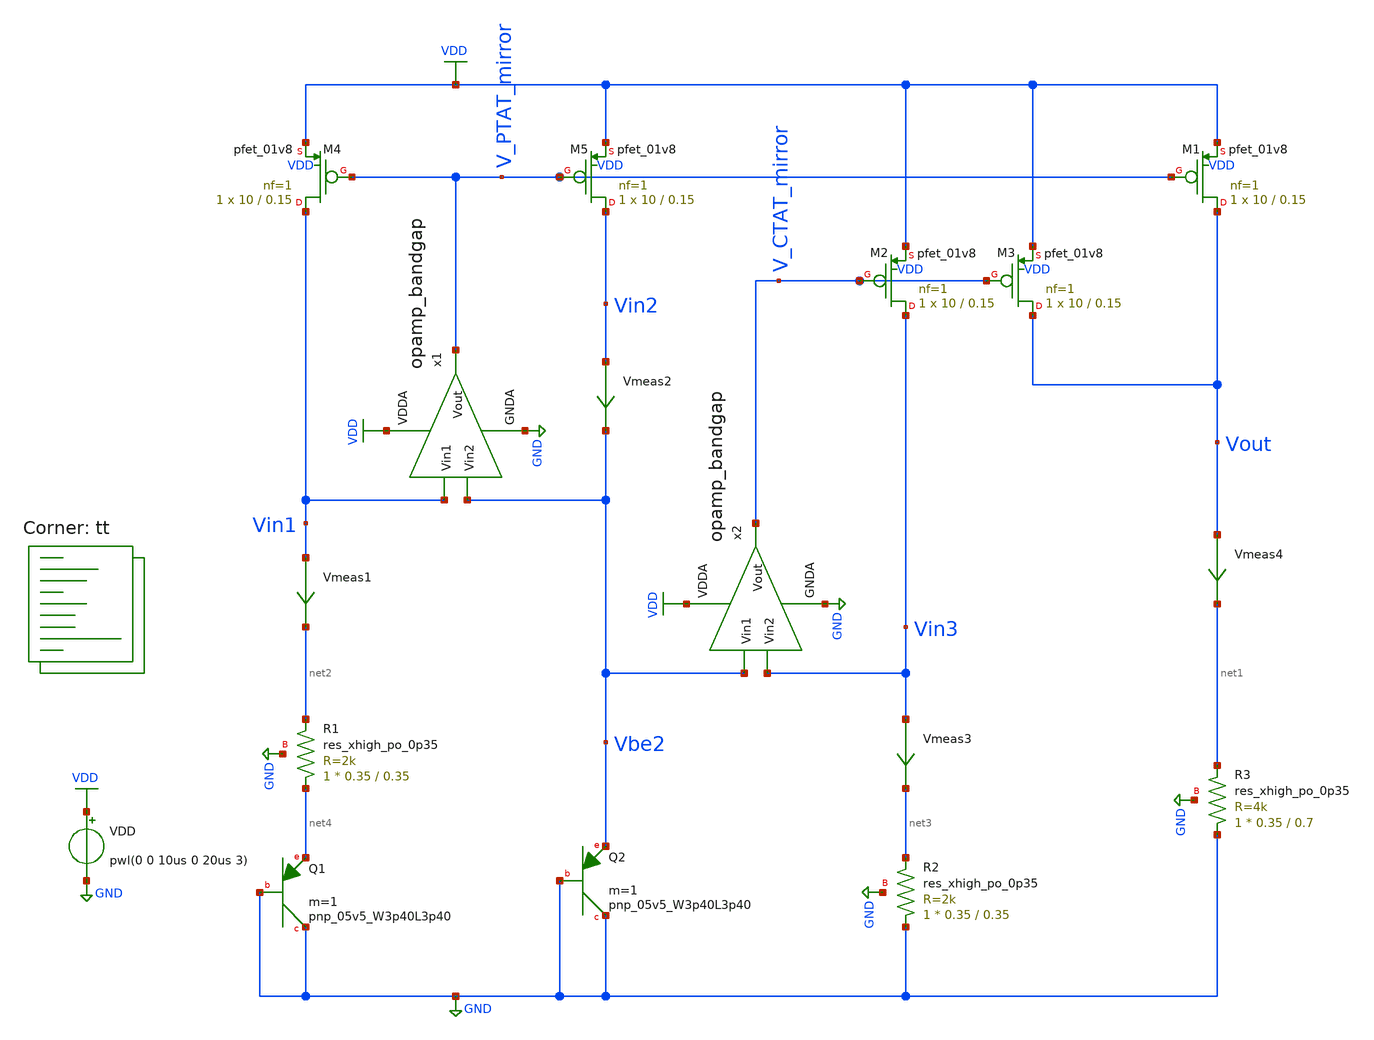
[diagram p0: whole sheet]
** sch_path: projects/pll/bandgapref/xschem_ngspice/mos_bandgap4.sch
**.subckt mos_bandgap4
XM4 Vin1 V_PTAT_mirror VDD VDD sky130_fd_pr__pfet_01v8 L=0.15 W=10 nf=1 ad='int((nf+1)/2) * W/nf * 0.29'
+ as='int((nf+2)/2) * W/nf * 0.29' pd='2*int((nf+1)/2) * (W/nf + 0.29)' ps='2*int((nf+2)/2) * (W/nf + 0.29)'
+ nrd='0.29 / W' nrs='0.29 / W' sa=0 sb=0 sd=0 mult=1 m=1
XM5 Vin2 V_PTAT_mirror VDD VDD sky130_fd_pr__pfet_01v8 L=0.15 W=10 nf=1 ad='int((nf+1)/2) * W/nf * 0.29'
+ as='int((nf+2)/2) * W/nf * 0.29' pd='2*int((nf+1)/2) * (W/nf + 0.29)' ps='2*int((nf+2)/2) * (W/nf + 0.29)'
+ nrd='0.29 / W' nrs='0.29 / W' sa=0 sb=0 sd=0 mult=1 m=1
XQ1 GND GND net4 sky130_fd_pr__pnp_05v5_W3p40L3p40 m=1
XQ2 GND GND Vbe2 sky130_fd_pr__pnp_05v5_W3p40L3p40 m=1
XM1 Vout V_PTAT_mirror VDD VDD sky130_fd_pr__pfet_01v8 L=0.15 W=10 nf=1 ad='int((nf+1)/2) * W/nf * 0.29'
+ as='int((nf+2)/2) * W/nf * 0.29' pd='2*int((nf+1)/2) * (W/nf + 0.29)' ps='2*int((nf+2)/2) * (W/nf + 0.29)'
+ nrd='0.29 / W' nrs='0.29 / W' sa=0 sb=0 sd=0 mult=1 m=1
Vmeas4 Vout net1 0
.save i(vmeas4)
x1 VDD V_PTAT_mirror Vbe2 Vin1 GND opamp_bandgap
Vmeas1 Vin1 net2 0
.save i(vmeas1)
Vmeas2 Vin2 Vbe2 0
.save i(vmeas2)
x2 VDD V_CTAT_mirror Vin3 Vbe2 GND opamp_bandgap
Vmeas3 Vin3 net3 0
.save i(vmeas3)
XM2 Vin3 V_CTAT_mirror VDD VDD sky130_fd_pr__pfet_01v8 L=0.15 W=10 nf=1 ad='int((nf+1)/2) * W/nf * 0.29'
+ as='int((nf+2)/2) * W/nf * 0.29' pd='2*int((nf+1)/2) * (W/nf + 0.29)' ps='2*int((nf+2)/2) * (W/nf + 0.29)'
+ nrd='0.29 / W' nrs='0.29 / W' sa=0 sb=0 sd=0 mult=1 m=1
XM3 Vout V_CTAT_mirror VDD VDD sky130_fd_pr__pfet_01v8 L=0.15 W=10 nf=1 ad='int((nf+1)/2) * W/nf * 0.29'
+ as='int((nf+2)/2) * W/nf * 0.29' pd='2*int((nf+1)/2) * (W/nf + 0.29)' ps='2*int((nf+2)/2) * (W/nf + 0.29)'
+ nrd='0.29 / W' nrs='0.29 / W' sa=0 sb=0 sd=0 mult=1 m=1
VDD VDD GND pwl(0 0 10us 0 20us 3)
XR1 net4 net2 GND sky130_fd_pr__res_xhigh_po_0p35 L=0.35 mult=1 m=1
XR2 GND net3 GND sky130_fd_pr__res_xhigh_po_0p35 L=0.35 mult=1 m=1
XR3 GND net1 GND sky130_fd_pr__res_xhigh_po_0p35 L=0.7 mult=1 m=1
**** begin user architecture code
.lib $::SKYWATER_MODELS/sky130.lib.spice tt



.option wnflag=1
.option method=gear

.control
  save all
   op
*  dc temp -40 120 2 VDD 1.8 3.3 0.2
  *dc VDD 0 3.3 0.1 temp -0 100 4
  tran 5ns 50us
  write mos_bandgap4.raw
  set appendwrite
.endc



**** end user architecture code
**.ends

* expanding   symbol:
*+  /foss/designs/my_design/projects/pll/bandgapref/xschem_ngspice/opamp_bandgap.sym # of pins=5
** sym_path: projects/pll/bandgapref/xschem_ngspice/opamp_bandgap.sym
** sch_path: projects/pll/bandgapref/xschem_ngspice/opamp_bandgap.sch
.subckt opamp_bandgap VDDA Vout Vin2 Vin1 GNDA
*.ipin Vin1
*.opin Vout
*.ipin Vin2
*.ipin GNDA
*.ipin VDDA
XM2 net1 Vin1 net2 GNDA sky130_fd_pr__nfet_01v8 L=0.15 W=1 nf=1 ad='int((nf+1)/2) * W/nf * 0.29' as='int((nf+2)/2) * W/nf * 0.29'
+ pd='2*int((nf+1)/2) * (W/nf + 0.29)' ps='2*int((nf+2)/2) * (W/nf + 0.29)' nrd='0.29 / W' nrs='0.29 / W'
+ sa=0 sb=0 sd=0 mult=1 m=1
XM3 Vout Vin2 net2 GNDA sky130_fd_pr__nfet_01v8 L=0.15 W=1 nf=1 ad='int((nf+1)/2) * W/nf * 0.29' as='int((nf+2)/2) * W/nf * 0.29'
+ pd='2*int((nf+1)/2) * (W/nf + 0.29)' ps='2*int((nf+2)/2) * (W/nf + 0.29)' nrd='0.29 / W' nrs='0.29 / W'
+ sa=0 sb=0 sd=0 mult=1 m=1
XM4 net1 net1 VDDA VDDA sky130_fd_pr__pfet_01v8 L=0.15 W=2 nf=1 ad='int((nf+1)/2) * W/nf * 0.29' as='int((nf+2)/2) * W/nf * 0.29'
+ pd='2*int((nf+1)/2) * (W/nf + 0.29)' ps='2*int((nf+2)/2) * (W/nf + 0.29)' nrd='0.29 / W' nrs='0.29 / W'
+ sa=0 sb=0 sd=0 mult=1 m=1
XM5 Vout net1 VDDA VDDA sky130_fd_pr__pfet_01v8 L=0.15 W=2 nf=1 ad='int((nf+1)/2) * W/nf * 0.29' as='int((nf+2)/2) * W/nf * 0.29'
+ pd='2*int((nf+1)/2) * (W/nf + 0.29)' ps='2*int((nf+2)/2) * (W/nf + 0.29)' nrd='0.29 / W' nrs='0.29 / W'
+ sa=0 sb=0 sd=0 mult=1 m=1
XM1 net2 net2 GNDA GNDA sky130_fd_pr__nfet_01v8 L=0.15 W=1 nf=1 ad='int((nf+1)/2) * W/nf * 0.29' as='int((nf+2)/2) * W/nf * 0.29'
+ pd='2*int((nf+1)/2) * (W/nf + 0.29)' ps='2*int((nf+2)/2) * (W/nf + 0.29)' nrd='0.29 / W' nrs='0.29 / W'
+ sa=0 sb=0 sd=0 mult=1 m=1
.ends

.GLOBAL GND
.GLOBAL VDD
.end
